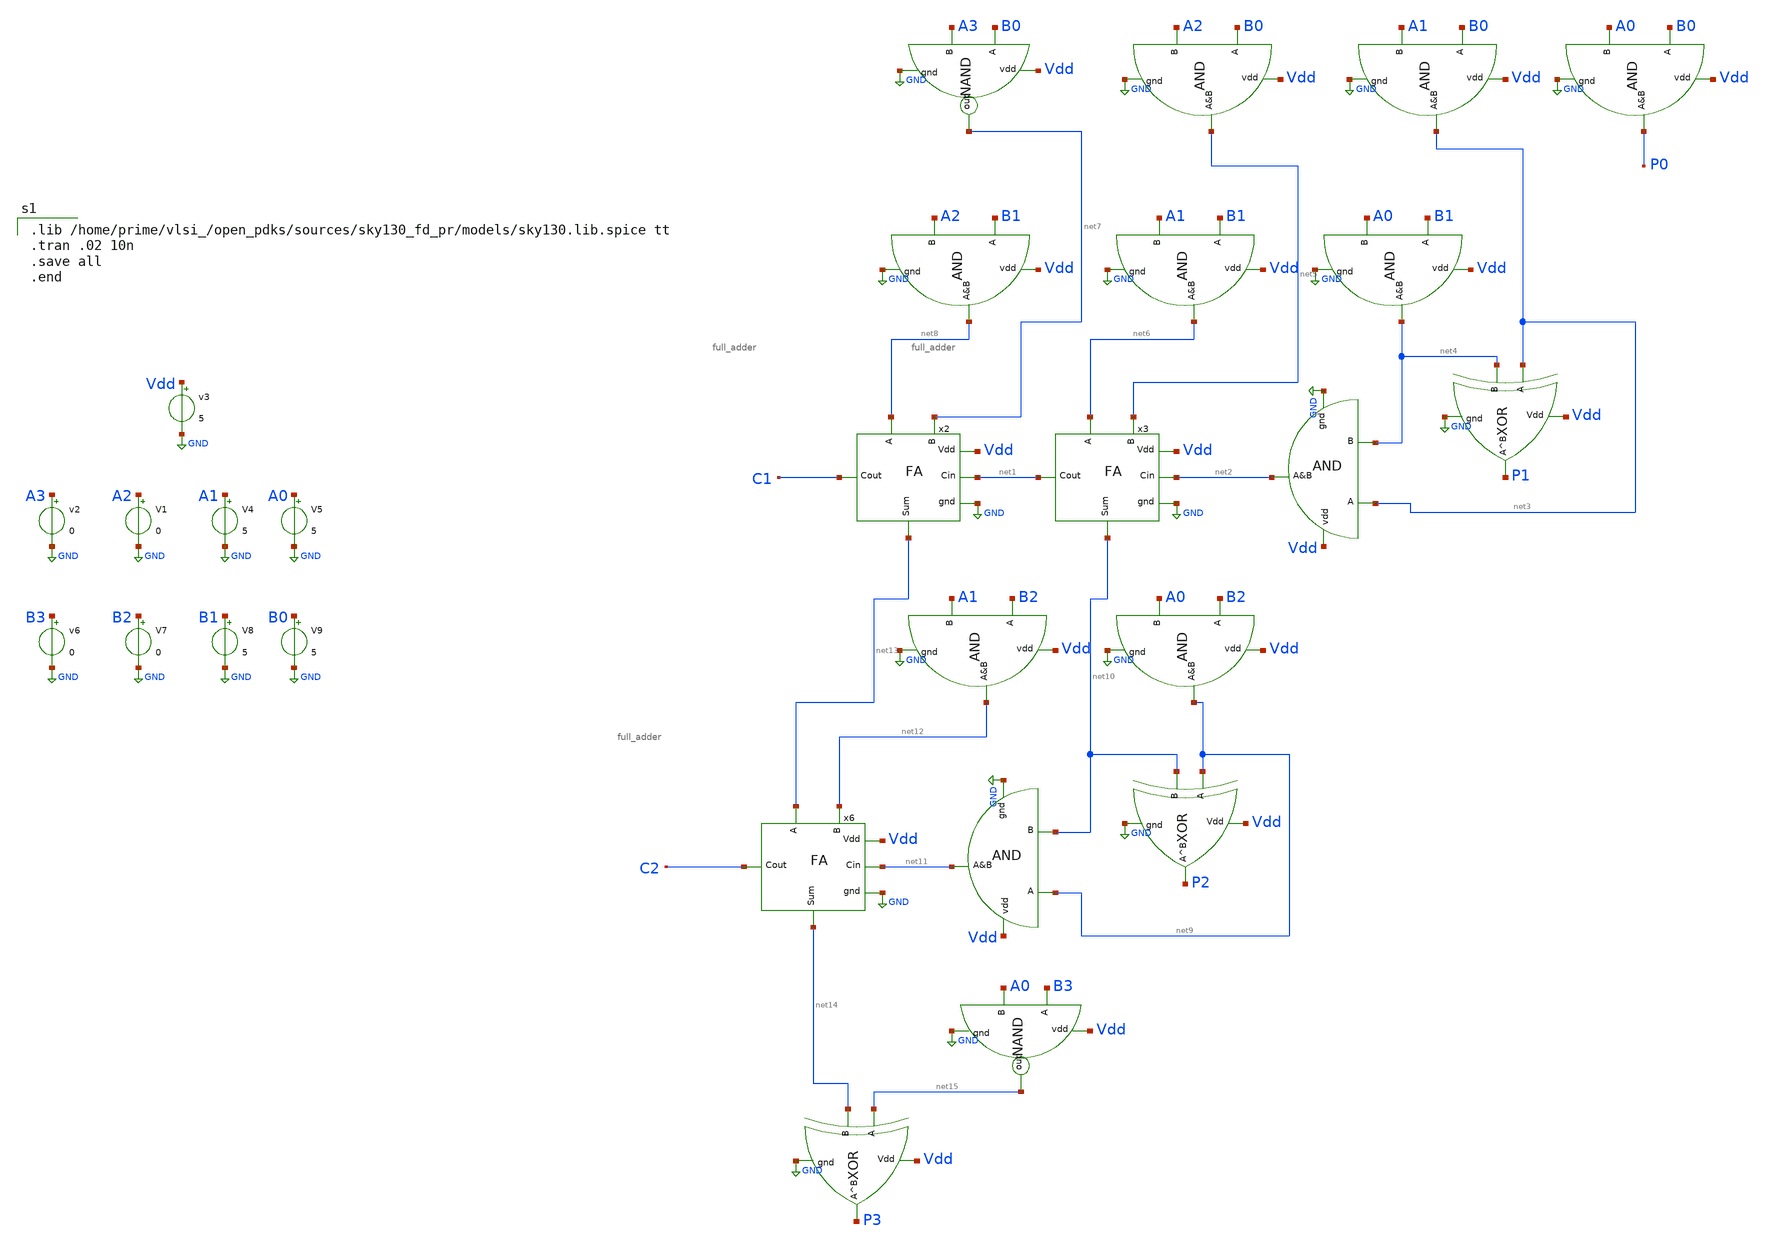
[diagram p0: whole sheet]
** sch_path: extra_stuff/sandbox.sch
**.subckt sandbox
v2 A3 GND 0
v3 Vdd GND 5
V1 A2 GND 0
x2 net13 C1 net1 Vdd GND net8 net7 full_adder
x3 net10 net1 net2 Vdd GND net6 net5 full_adder
x6 net14 C2 net11 Vdd GND net13 net12 full_adder
x10 Vdd GND P1 net3 net4 xor
x11 net3 net4 net2 Vdd GND and
x7 net7 Vdd B0 A3 GND NAND
x8 B0 A2 net5 Vdd GND and
x9 B0 A1 net3 Vdd GND and
x12 B0 A0 P0 Vdd GND and
x14 B1 A2 net8 Vdd GND and
x15 B1 A1 net6 Vdd GND and
x16 B1 A0 net4 Vdd GND and
x19 B2 A1 net12 Vdd GND and
x20 B2 A0 net9 Vdd GND and
x25 Vdd GND P2 net9 net10 xor
x26 net9 net10 net11 Vdd GND and
x27 Vdd GND P3 net15 net14 xor
x21 net15 Vdd B3 A0 GND NAND
V4 A1 GND 5
V5 A0 GND 5
v6 B3 GND 0
V7 B2 GND 0
V8 B1 GND 5
V9 B0 GND 5
**** begin user architecture code

.lib /home/prime/vlsi_/open_pdks/sources/sky130_fd_pr/models/sky130.lib.spice tt
.tran .02 10n
.save all
.end

**** end user architecture code
**.ends
.GLOBAL GND
.end
